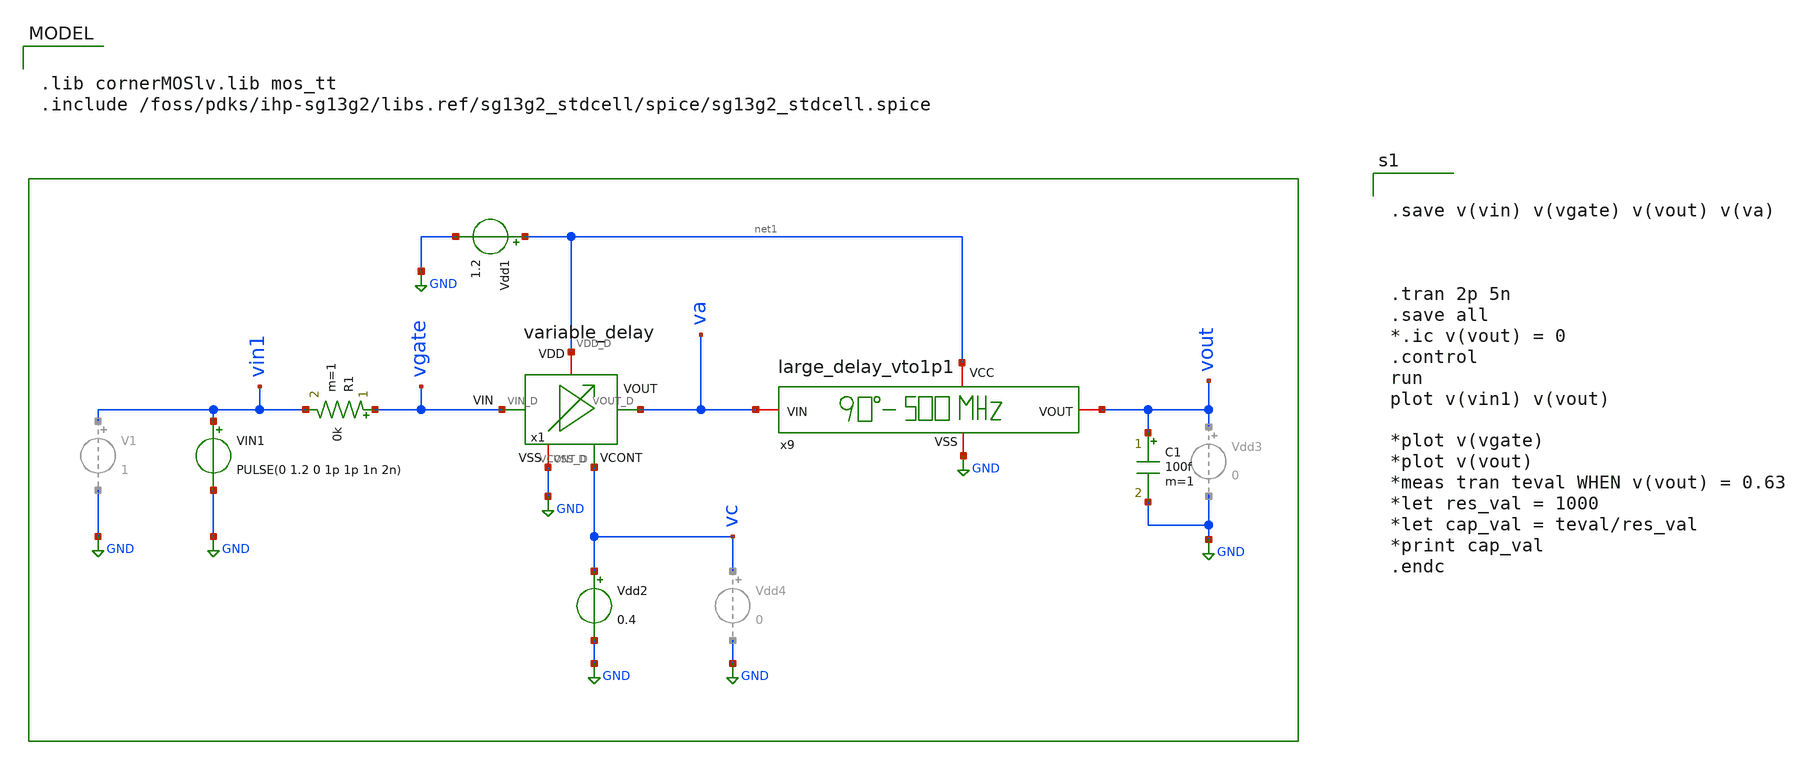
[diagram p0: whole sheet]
** sch_path: sch/delay_variable_line/tb_QVDL_500MHZ.sch
**.subckt tb_QVDL_500MHZ
x1 net1 vgate va vc GND variable_delay
R1 vgate vin1 0k m=1
Vdd1 net1 GND 1.2
Vdd2 vc GND 0.4
C1 vout GND 100f m=1
VIN1 vin1 GND PULSE(0 1.2 0 1p 1p 1n 2n)
x9 net1 GND va vout large_delay_vto1p1
**** begin user architecture code


.save v(vin) v(vgate) v(vout) v(va)



.tran 2p 5n
.save all
*.ic v(vout) = 0
.control
run
plot v(vin1) v(vout)

*plot v(vgate)
*plot v(vout)
*meas tran teval WHEN v(vout) = 0.63
*let res_val = 1000
*let cap_val = teval/res_val
*print cap_val
.endc



.lib cornerMOSlv.lib mos_tt
.include /foss/pdks/ihp-sg13g2/libs.ref/sg13g2_stdcell/spice/sg13g2_stdcell.spice

**** end user architecture code
**.ends

* expanding   symbol:  /foss/designs/DLL/variable_delay.sym # of pins=5
** sym_path: sch/delay_variable_line/variable_delay.sym
** sch_path: sch/delay_variable_line/variable_delay.sch
.subckt variable_delay VDD_D VIN_D VOUT_D VCONT_D VSS_D
*.iopin VSS_D
*.iopin VDD_D
*.ipin VIN_D
*.opin VOUT_D
*.ipin VCONT_D
XM3 net4 VCONT_D net2 net2 sg13_lv_nmos w=1u l=0.13u ng=1 m=1 mm_ok=1
XM5 net3 VCONT_D net2 net2 sg13_lv_nmos w=1u l=5u ng=1 m=1 mm_ok=1
XM4 net4 net4 VDD_D VDD_D sg13_lv_pmos w=1u l=0.13u ng=1 m=1 mm_ok=1
XM6 net1 net4 VDD_D VDD_D sg13_lv_pmos w=1u l=5u ng=1 m=1 mm_ok=1
XM2 VOUT_D VIN_D net1 VDD_D sg13_lv_pmos w=10u l=10u ng=1 m=1 mm_ok=1
XM1 VOUT_D VIN_D net3 net2 sg13_lv_nmos w=10u l=10u ng=1 m=1 mm_ok=1
.ends


* expanding   symbol:
*+  /foss/designs/UCU/uniccass-icdesign-tools/shared_xserver/OS_AnalogIC_UCU_July2025/Day3/large_delay/large_delay_vto1p1.sym # of pins=4
** sym_path: sch/large_delay_vto1p1/large_delay_vto1p1.sym
** sch_path: sch/large_delay_vto1p1/large_delay_vto1p1.sch
.subckt large_delay_vto1p1 VCC VSS VIN VOUT
*.iopin VIN
*.iopin VOUT
*.iopin VCC
*.iopin VSS
x1 VOUT VIN VCC VSS sg13g2_dlygate4sd1_1
x2 VOUT VIN VCC VSS sg13g2_dlygate4sd1_1
x3 VOUT VIN VCC VSS sg13g2_dlygate4sd1_1
x4 VOUT VIN VCC VSS sg13g2_dlygate4sd1_1
.ends


* expanding   symbol:  sg13g2_stdcells/sg13g2_dlygate4sd3_1.sym # of pins=2
** sym_path: sg13g2_stdcells/sg13g2_dlygate4sd3_1.sym
** sch_path: sg13g2_stdcells/sg13g2_dlygate4sd3_1.sch
.subckt sg13g2_dlygate4sd3_1 X A VDD VSS
*.ipin A
*.opin X
*.iopin VDD
*.iopin VSS
XM1 net3 A VSS VSS sg13_lv_nmos w=420.00n l=130.00n ng=1 m=1 mm_ok=1
XM2 net1 net3 VSS VSS sg13_lv_nmos w=420.00n l=500.0n ng=1 m=1 mm_ok=1
XM3 net2 net1 VSS VSS sg13_lv_nmos w=420.00n l=500.0n ng=1 m=1 mm_ok=1
XM4 X net2 VSS VSS sg13_lv_nmos w=740.00n l=130.00n ng=1 m=1 mm_ok=1
XM5 net3 A VDD VDD sg13_lv_pmos w=420.00n l=130.00n ng=1 m=1 mm_ok=1
XM6 net1 net3 VDD VDD sg13_lv_pmos w=1.000u l=500.0n ng=1 m=1 mm_ok=1
XM7 net2 net1 VDD VDD sg13_lv_pmos w=1.000u l=500.0n ng=1 m=1 mm_ok=1
XM8 X net2 VDD VDD sg13_lv_pmos w=1.12u l=130.00n ng=1 m=1 mm_ok=1
.ends


* expanding   symbol:  sg13g2_stdcells/sg13g2_dlygate4sd1_1.sym # of pins=2
** sym_path: sg13g2_stdcells/sg13g2_dlygate4sd1_1.sym
** sch_path: sg13g2_stdcells/sg13g2_dlygate4sd1_1.sch
.subckt sg13g2_dlygate4sd1_1 X A VDD VSS
*.ipin A
*.opin X
*.iopin VDD
*.iopin VSS
XM1 net2 A VSS VSS sg13_lv_nmos w=420.00n l=130.00n ng=1 m=1 mm_ok=1
XM2 net1 net2 VSS VSS sg13_lv_nmos w=420.00n l=130.00n ng=1 m=1 mm_ok=1
XM3 net3 net1 VSS VSS sg13_lv_nmos w=420.00n l=130.00n ng=1 m=1 mm_ok=1
XM4 X net3 VSS VSS sg13_lv_nmos w=740.00n l=130.00n ng=1 m=1 mm_ok=1
XM5 net2 A VDD VDD sg13_lv_pmos w=420.00n l=130.00n ng=1 m=1 mm_ok=1
XM6 net1 net2 VDD VDD sg13_lv_pmos w=1.000u l=130.00n ng=1 m=1 mm_ok=1
XM7 net3 net1 VDD VDD sg13_lv_pmos w=1.000u l=130.00n ng=1 m=1 mm_ok=1
XM8 X net3 VDD VDD sg13_lv_pmos w=1.12u l=130.00n ng=1 m=1 mm_ok=1
.ends

.GLOBAL GND
.end
